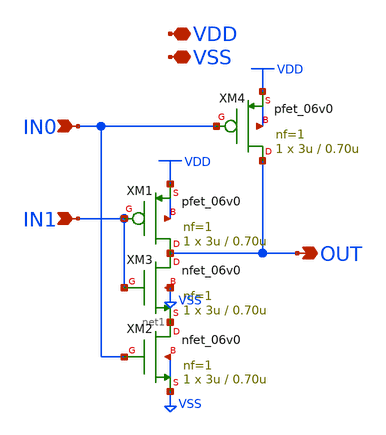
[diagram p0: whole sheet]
** sch_path: io_nand2_1.sch
* Copyright 2023 David Mitchell Bailey
* Licensed under the Apache License, Version 2.0 (the "License");
* you may not use this file except in compliance with the License.
* You may obtain a copy of the License at
* https://www.apache.org/licenses/LICENSE-2.0
* Unless required by applicable law or agreed to in writing, software
* distributed under the License is distributed on an "AS IS" BASIS,
* WITHOUT WARRANTIES OR CONDITIONS OF ANY KIND, either express or implied.
* See the License for the specific language governing permissions and
* limitations under the License.
**.subckt io_nand2_1 OUT IN0 IN1 VDD VSS
*.opin OUT
*.ipin IN0
*.ipin IN1
*.iopin VDD
*.iopin VSS
XM1 OUT IN1 VDD VDD pfet_06v0 L=0.70u W=3u nf=1 ad='int((nf+1)/2) * W/nf * 0.18u' as='int((nf+2)/2) * W/nf * 0.18u'
+ pd='2*int((nf+1)/2) * (W/nf + 0.18u)' ps='2*int((nf+2)/2) * (W/nf + 0.18u)' nrd='0.18u / W' nrs='0.18u / W'
+ sa=0 sb=0 sd=0 m=1
XM2 net1 IN0 VSS VSS nfet_06v0 L=0.70u W=3u nf=1 ad='int((nf+1)/2) * W/nf * 0.18u' as='int((nf+2)/2) * W/nf * 0.18u'
+ pd='2*int((nf+1)/2) * (W/nf + 0.18u)' ps='2*int((nf+2)/2) * (W/nf + 0.18u)' nrd='0.18u / W' nrs='0.18u / W'
+ sa=0 sb=0 sd=0 m=1
XM3 OUT IN1 net1 VSS nfet_06v0 L=0.70u W=3u nf=1 ad='int((nf+1)/2) * W/nf * 0.18u' as='int((nf+2)/2) * W/nf * 0.18u'
+ pd='2*int((nf+1)/2) * (W/nf + 0.18u)' ps='2*int((nf+2)/2) * (W/nf + 0.18u)' nrd='0.18u / W' nrs='0.18u / W'
+ sa=0 sb=0 sd=0 m=1
XM4 OUT IN0 VDD VDD pfet_06v0 L=0.70u W=3u nf=1 ad='int((nf+1)/2) * W/nf * 0.18u' as='int((nf+2)/2) * W/nf * 0.18u'
+ pd='2*int((nf+1)/2) * (W/nf + 0.18u)' ps='2*int((nf+2)/2) * (W/nf + 0.18u)' nrd='0.18u / W' nrs='0.18u / W'
+ sa=0 sb=0 sd=0 m=1
**.ends
.GLOBAL VDD
.end
